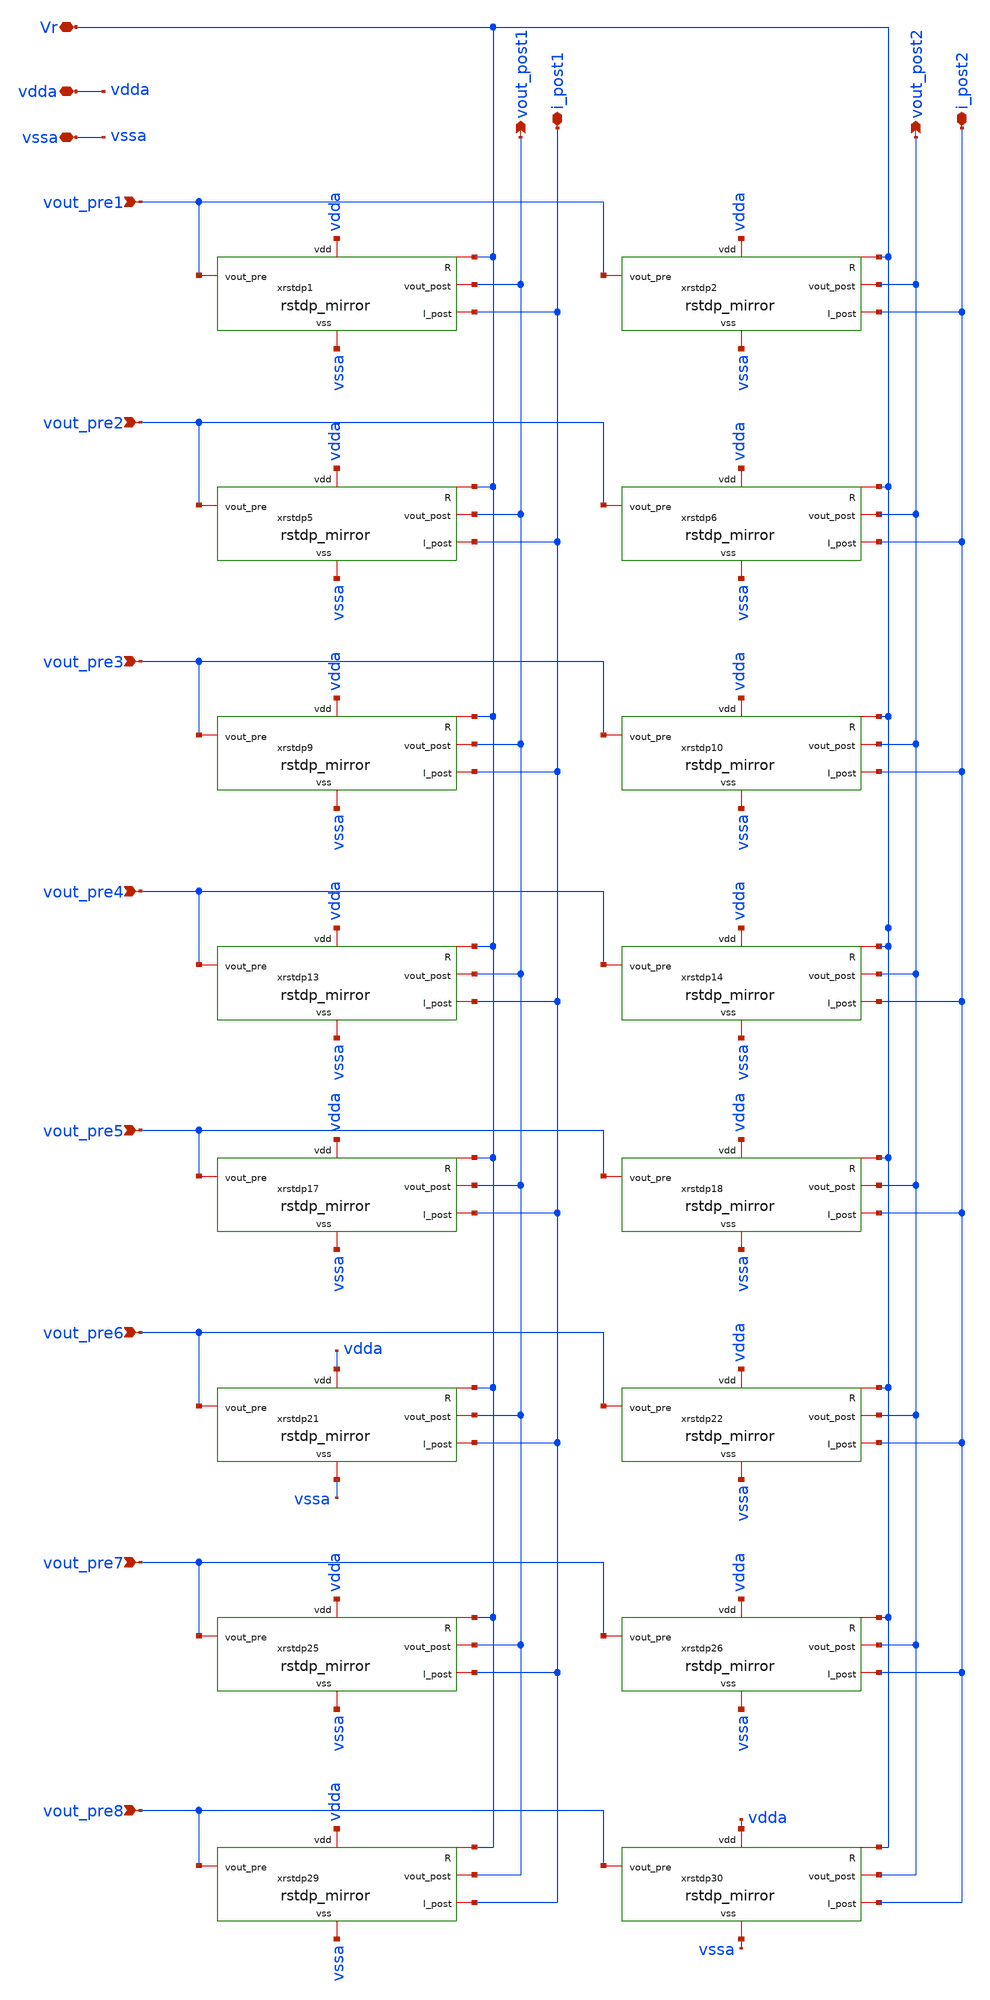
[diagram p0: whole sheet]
** sch_path: Synapse/rstdp_array_8x2.sch
**.subckt rstdp_array_8x2 vout_pre1 vout_post1 vdda vssa i_post1 vout_pre2 vout_pre3 vout_pre4
*+ vout_post2 i_post2 Vr vout_pre5 vout_pre6 vout_pre7 vout_pre8
*.ipin vout_pre1
*.opin vout_post1
*.iopin vdda
*.iopin vssa
*.iopin i_post1
*.ipin vout_pre2
*.ipin vout_pre3
*.ipin vout_pre4
*.opin vout_post2
*.iopin i_post2
*.iopin Vr
*.ipin vout_pre5
*.ipin vout_pre6
*.ipin vout_pre7
*.ipin vout_pre8
xrstdp1 vdda Vr vssa vout_pre1 vout_post1 i_post1 rstdp_mirror
xrstdp2 vdda Vr vssa vout_pre1 vout_post2 i_post2 rstdp_mirror
xrstdp5 vdda Vr vssa vout_pre2 vout_post1 i_post1 rstdp_mirror
xrstdp6 vdda Vr vssa vout_pre2 vout_post2 i_post2 rstdp_mirror
xrstdp9 vdda Vr vssa vout_pre3 vout_post1 i_post1 rstdp_mirror
xrstdp10 vdda Vr vssa vout_pre3 vout_post2 i_post2 rstdp_mirror
xrstdp13 vdda Vr vssa vout_pre4 vout_post1 i_post1 rstdp_mirror
xrstdp14 vdda Vr vssa vout_pre4 vout_post2 i_post2 rstdp_mirror
xrstdp17 vdda Vr vssa vout_pre5 vout_post1 i_post1 rstdp_mirror
xrstdp18 vdda Vr vssa vout_pre5 vout_post2 i_post2 rstdp_mirror
xrstdp21 vdda Vr vssa vout_pre6 vout_post1 i_post1 rstdp_mirror
xrstdp22 vdda Vr vssa vout_pre6 vout_post2 i_post2 rstdp_mirror
xrstdp25 vdda Vr vssa vout_pre7 vout_post1 i_post1 rstdp_mirror
xrstdp26 vdda Vr vssa vout_pre7 vout_post2 i_post2 rstdp_mirror
xrstdp29 vdda Vr vssa vout_pre8 vout_post1 i_post1 rstdp_mirror
xrstdp30 vdda Vr vssa vout_pre8 vout_post2 i_post2 rstdp_mirror
**.ends

* expanding   symbol:  Synapse/rstdp_mirror.sym # of pins=6
** sym_path: Synapse/rstdp_mirror.sym
** sch_path: Synapse/rstdp_mirror.sch
.subckt rstdp_mirror vdd R vss vout_pre vout_post I_post
*.iopin vdd
*.iopin vss
*.iopin R
*.iopin vout_post
*.iopin vout_pre
*.iopin I_post
XM2 A vout_pre vpre vss sky130_fd_pr__nfet_01v8 L=0.15 W=7.5 nf=1 ad='int((nf+1)/2) * W/nf * 0.29' as='int((nf+2)/2) * W/nf * 0.29'
+ pd='2*int((nf+1)/2) * (W/nf + 0.29)' ps='2*int((nf+2)/2) * (W/nf + 0.29)' nrd='0.29 / W' nrs='0.29 / W'
+ sa=0 sb=0 sd=0 mult=1 m=1
XM3 vpre vout_post vss vss sky130_fd_pr__nfet_01v8 L=0.15 W=7.5 nf=1 ad='int((nf+1)/2) * W/nf * 0.29'
+ as='int((nf+2)/2) * W/nf * 0.29' pd='2*int((nf+1)/2) * (W/nf + 0.29)' ps='2*int((nf+2)/2) * (W/nf + 0.29)'
+ nrd='0.29 / W' nrs='0.29 / W' sa=0 sb=0 sd=0 mult=1 m=1
XM1 A vout_post vpost vss sky130_fd_pr__nfet_01v8 L=0.15 W=7.5 nf=1 ad='int((nf+1)/2) * W/nf * 0.29'
+ as='int((nf+2)/2) * W/nf * 0.29' pd='2*int((nf+1)/2) * (W/nf + 0.29)' ps='2*int((nf+2)/2) * (W/nf + 0.29)'
+ nrd='0.29 / W' nrs='0.29 / W' sa=0 sb=0 sd=0 mult=1 m=1
XM4 vpost vout_pre vss vss sky130_fd_pr__nfet_01v8 L=0.15 W=7.5 nf=1 ad='int((nf+1)/2) * W/nf * 0.29'
+ as='int((nf+2)/2) * W/nf * 0.29' pd='2*int((nf+1)/2) * (W/nf + 0.29)' ps='2*int((nf+2)/2) * (W/nf + 0.29)'
+ nrd='0.29 / W' nrs='0.29 / W' sa=0 sb=0 sd=0 mult=1 m=1
XR2 te be rram_v0
XM5 vpre R be vss sky130_fd_pr__nfet_01v8 L=0.15 W=7.5 nf=1 ad='int((nf+1)/2) * W/nf * 0.29' as='int((nf+2)/2) * W/nf * 0.29'
+ pd='2*int((nf+1)/2) * (W/nf + 0.29)' ps='2*int((nf+2)/2) * (W/nf + 0.29)' nrd='0.29 / W' nrs='0.29 / W'
+ sa=0 sb=0 sd=0 mult=1 m=1
XM6 net1 R vpost vss sky130_fd_pr__nfet_01v8 L=0.15 W=7.5 nf=1 ad='int((nf+1)/2) * W/nf * 0.29' as='int((nf+2)/2) * W/nf * 0.29'
+ pd='2*int((nf+1)/2) * (W/nf + 0.29)' ps='2*int((nf+2)/2) * (W/nf + 0.29)' nrd='0.29 / W' nrs='0.29 / W'
+ sa=0 sb=0 sd=0 mult=1 m=1
XM7 vpre R net1 vdd sky130_fd_pr__pfet_01v8 L=0.15 W=15 nf=1 ad='int((nf+1)/2) * W/nf * 0.29' as='int((nf+2)/2) * W/nf * 0.29'
+ pd='2*int((nf+1)/2) * (W/nf + 0.29)' ps='2*int((nf+2)/2) * (W/nf + 0.29)' nrd='0.29 / W' nrs='0.29 / W'
+ sa=0 sb=0 sd=0 mult=1 m=1
XM8 be R vpost vdd sky130_fd_pr__pfet_01v8 L=0.15 W=15 nf=1 ad='int((nf+1)/2) * W/nf * 0.29' as='int((nf+2)/2) * W/nf * 0.29'
+ pd='2*int((nf+1)/2) * (W/nf + 0.29)' ps='2*int((nf+2)/2) * (W/nf + 0.29)' nrd='0.29 / W' nrs='0.29 / W'
+ sa=0 sb=0 sd=0 mult=1 m=1
XM14 net2 A vdd vdd sky130_fd_pr__pfet_01v8 L=0.5 W=2 nf=1 ad='int((nf+1)/2) * W/nf * 0.29' as='int((nf+2)/2) * W/nf * 0.29'
+ pd='2*int((nf+1)/2) * (W/nf + 0.29)' ps='2*int((nf+2)/2) * (W/nf + 0.29)' nrd='0.29 / W' nrs='0.29 / W'
+ sa=0 sb=0 sd=0 mult=1 m=1
XM15 A A vdd vdd sky130_fd_pr__pfet_01v8 L=0.15 W=10 nf=1 ad='int((nf+1)/2) * W/nf * 0.29' as='int((nf+2)/2) * W/nf * 0.29'
+ pd='2*int((nf+1)/2) * (W/nf + 0.29)' ps='2*int((nf+2)/2) * (W/nf + 0.29)' nrd='0.29 / W' nrs='0.29 / W'
+ sa=0 sb=0 sd=0 mult=1 m=1
**** begin user architecture code


.save v(te) v(be) i(vmr)


**** end user architecture code
Vmr te net1 0
.save i(vmr)
XM9 net2 vdd I_post vss sky130_fd_pr__nfet_01v8 L=0.15 W=1 nf=1 ad='int((nf+1)/2) * W/nf * 0.29' as='int((nf+2)/2) * W/nf * 0.29'
+ pd='2*int((nf+1)/2) * (W/nf + 0.29)' ps='2*int((nf+2)/2) * (W/nf + 0.29)' nrd='0.29 / W' nrs='0.29 / W'
+ sa=0 sb=0 sd=0 mult=1 m=1
.ends

.end
